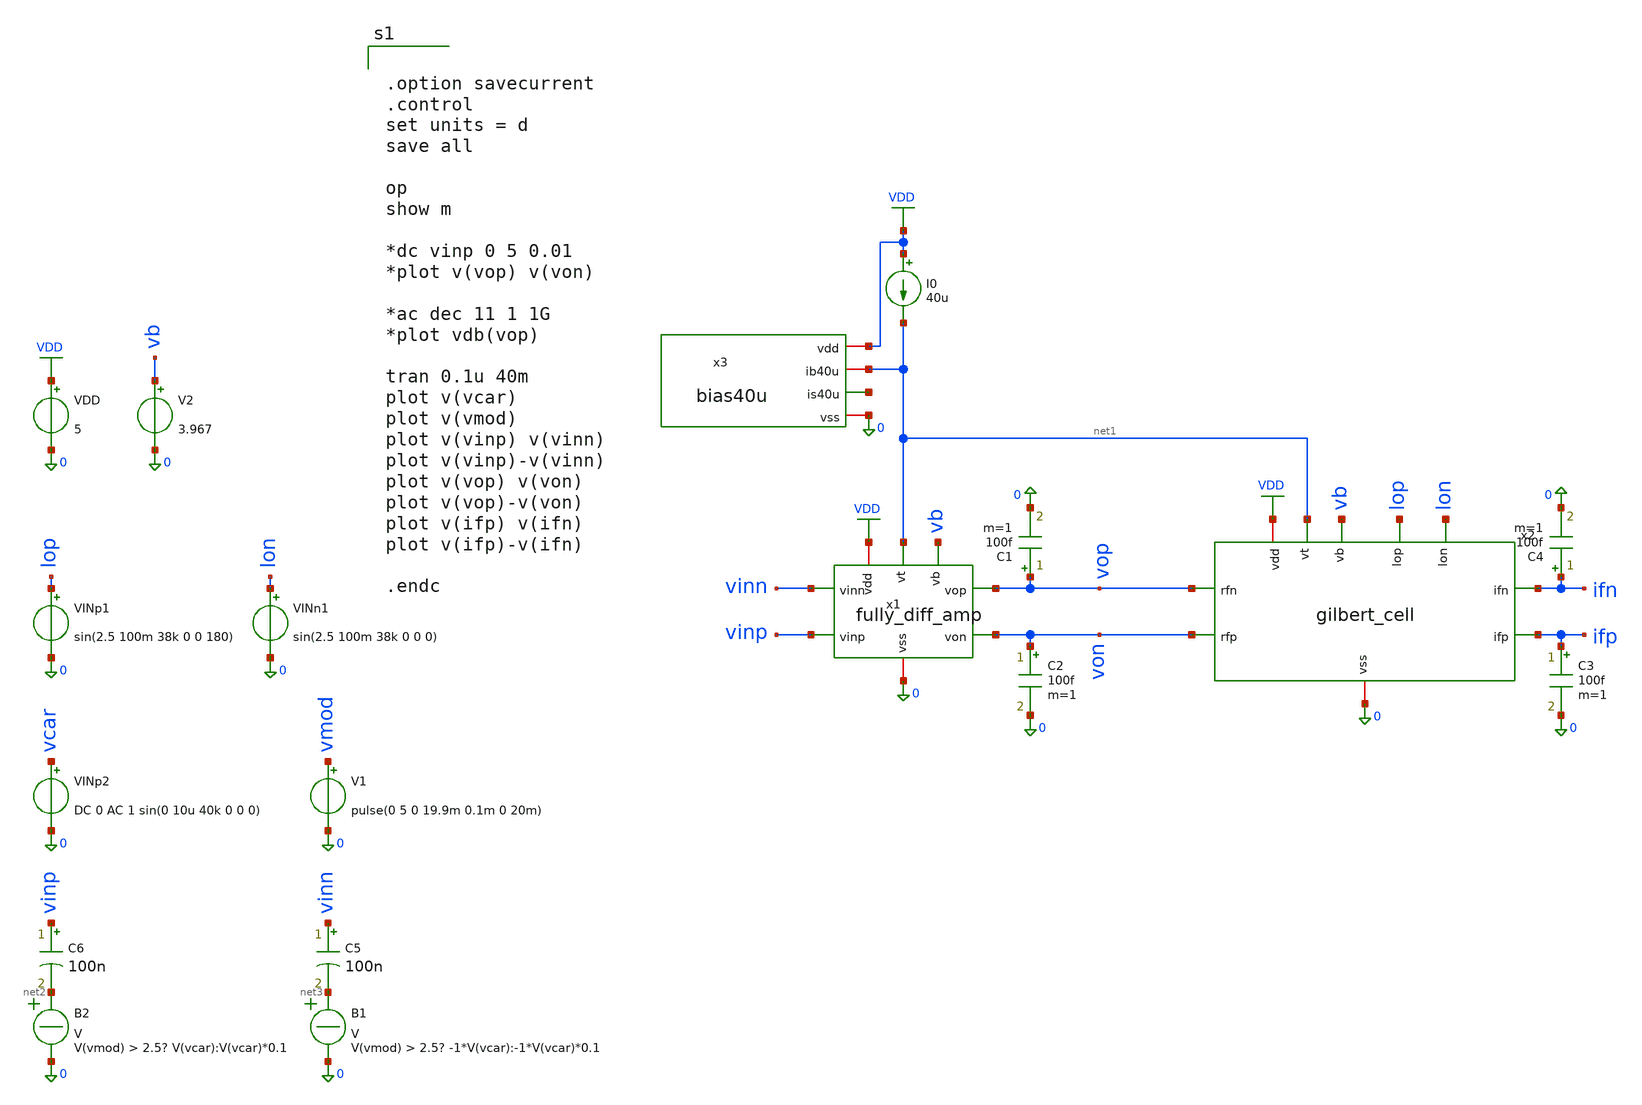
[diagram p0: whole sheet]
** sch_path: member_project/JJY_Receiver/Masahiro/jjy_recv/system_sim/cat.sch
**.subckt cat
VDD VDD 0 5
V2 vb 0 3.967
I0 VDD net1 40u
C1 vop 0 100f m=1
C2 von 0 100f m=1
x1 vb VDD vop von 0 vinn vinp net1 fully_diff_amp
x2 vb ifn VDD ifp 0 lop lon vop von net1 gilbert_cell
VINp1 lop 0 sin(2.5 100m 38k 0 0 180)
VINn1 lon 0 sin(2.5 100m 38k 0 0 0)
VINp2 vcar 0 DC 0 AC 1 sin(0 10u 40k 0 0 0)
V1 vmod 0 pulse(0 5 0 19.9m 0.1m 0 20m)
B2 net2 0 V = V(vmod) > 2.5? V(vcar):V(vcar)*0.1
B1 net3 0 V = V(vmod) > 2.5? -1*V(vcar):-1*V(vcar)*0.1
C5 vinn net3 100n m=1
C6 vinp net2 100n m=1
C3 ifp 0 100f m=1
C4 ifn 0 100f m=1
x3 VDD net1 net4 0 bias40u
**** begin user architecture code
 .include $::LIB/ip62_models


.option savecurrent
.control
set units = d
save all

op
show m

*dc vinp 0 5 0.01
*plot v(vop) v(von)

*ac dec 11 1 1G
*plot vdb(vop)

tran 0.1u 40m
plot v(vcar)
plot v(vmod)
plot v(vinp) v(vinn)
plot v(vinp)-v(vinn)
plot v(vop) v(von)
plot v(vop)-v(von)
plot v(ifp) v(ifn)
plot v(ifp)-v(ifn)

.endc


**** end user architecture code
**.ends

* expanding   symbol:  fully_diff_amp.sym # of pins=8
** sym_path: member_project/JJY_Receiver/Masahiro/jjy_recv/diff_amp/fully_diff_amp.sym
** sch_path: member_project/JJY_Receiver/Masahiro/jjy_recv/diff_amp/fully_diff_amp.sch
.subckt fully_diff_amp vb vdd vop von vss vinn vinp vt
*.opin vop
*.opin von
*.ipin vinp
*.ipin vb
*.ipin vt
*.ipin vinn
*.iopin vdd
*.iopin vss
XM1 vop vb vdd vdd PMOS w=45u l=2u as=0 ad=0 ps=0 pd=0 nrd=0 nrs=0 m=1
XM2 von vb vdd vdd PMOS w=45u l=2u as=0 ad=0 ps=0 pd=0 nrd=0 nrs=0 m=1
XM3 net1 vt vss vss NMOS w=10u l=2u as=0 ad=0 ps=0 pd=0 nrd=0 nrs=0 m=2
XM7 von vinp net1 vss NMOS w=20u l=2u as=0 ad=0 ps=0 pd=0 nrd=0 nrs=0 m=1
XM8 vop vinn net1 vss NMOS w=20u l=2u as=0 ad=0 ps=0 pd=0 nrd=0 nrs=0 m=1
XM6 net2 net2 vop vdd PMOS w=45u l=8u as=0 ad=0 ps=0 pd=0 nrd=0 nrs=0 m=1
XM9 net2 net2 vinn vdd PMOS w=45u l=8u as=0 ad=0 ps=0 pd=0 nrd=0 nrs=0 m=1
XM5 net3 net3 von vdd PMOS w=45u l=8u as=0 ad=0 ps=0 pd=0 nrd=0 nrs=0 m=1
XM10 net3 net3 vinp vdd PMOS w=45u l=8u as=0 ad=0 ps=0 pd=0 nrd=0 nrs=0 m=1
XM12 vinn vinn vss vss NMOS w=12.6u l=8u as=0 ad=0 ps=0 pd=0 nrd=0 nrs=0 m=1
XM13 vinn vinn vdd vdd PMOS w=34.4u l=8u as=0 ad=0 ps=0 pd=0 nrd=0 nrs=0 m=1
XM11 vinp vinp vss vss NMOS w=12.6u l=8u as=0 ad=0 ps=0 pd=0 nrd=0 nrs=0 m=1
XM14 vinp vinp vdd vdd PMOS w=34.4u l=8u as=0 ad=0 ps=0 pd=0 nrd=0 nrs=0 m=1
.ends


* expanding   symbol:
*+  /home/ishi-kai/ISHI-KAI_Multiple_Projects_OpenMPW_OpenSUSI-TR10-1/member_project/JJY_Receiver/Masahiro/jjy_recv/gilbert_cell/gilbert_cell.sym # of pins=10
** sym_path: member_project/JJY_Receiver/Masahiro/jjy_recv/gilbert_cell/gilbert_cell.sym
** sch_path: member_project/JJY_Receiver/Masahiro/jjy_recv/gilbert_cell/gilbert_cell.sch
.subckt gilbert_cell vb ifn vdd ifp vss lop lon rfn rfp vt
*.opin ifp
*.opin ifn
*.ipin rfp
*.ipin vb
*.ipin vt
*.ipin rfn
*.iopin vdd
*.iopin vss
*.ipin lon
*.ipin lop
XM1 ifp vb vdd vdd PMOS w=45u l=2u as=0 ad=0 ps=0 pd=0 nrd=0 nrs=0 m=1
XM2 ifn vb vdd vdd PMOS w=45u l=2u as=0 ad=0 ps=0 pd=0 nrd=0 nrs=0 m=1
XM3 net3 vt vss vss NMOS w=10u l=2u as=0 ad=0 ps=0 pd=0 nrd=0 nrs=0 m=2
XM7 net1 rfp net3 vss NMOS w=20u l=2u as=0 ad=0 ps=0 pd=0 nrd=0 nrs=0 m=1
XM8 net2 rfn net3 vss NMOS w=20u l=2u as=0 ad=0 ps=0 pd=0 nrd=0 nrs=0 m=1
XM5 ifn lop net1 vss NMOS w=20u l=2u as=0 ad=0 ps=0 pd=0 nrd=0 nrs=0 m=1
XM6 ifp lon net1 vss NMOS w=20u l=2u as=0 ad=0 ps=0 pd=0 nrd=0 nrs=0 m=1
XM9 ifn lon net2 vss NMOS w=20u l=2u as=0 ad=0 ps=0 pd=0 nrd=0 nrs=0 m=1
XM10 ifp lop net2 vss NMOS w=20u l=2u as=0 ad=0 ps=0 pd=0 nrd=0 nrs=0 m=1
.ends


* expanding   symbol:
*+  /home/ishi-kai/ISHI-KAI_Multiple_Projects_OpenMPW_OpenSUSI-TR10-1/member_project/JJY_Receiver/Masahiro/jjy_recv/bias_for_mix_amp/bias40u.sym # of pins=4
** sym_path: member_project/JJY_Receiver/Masahiro/jjy_recv/bias_for_mix_amp/bias40u.sym
** sch_path: member_project/JJY_Receiver/Masahiro/jjy_recv/bias_for_mix_amp/bias40u.sch
.subckt bias40u vdd ib40u is40u vss
*.iopin vss
*.iopin ib40u
*.iopin vdd
*.opin is40u
XXM1 ib40u ib40u vss vss NMOS w=10u l=2u nrd=0 nrs=0 m=2
XXM2 net1 ib40u vss vss NMOS w=10u l=2u nrd=0 nrs=0 m=2
XXM3 net1 vdd vdd vdd PMOS w=45u l=2u nrd=0 nrs=0 m=1
XXM4 is40u vdd vdd vdd PMOS w=45u l=2u nrd=0 nrs=0 m=1
.ends

.GLOBAL VDD
.end
